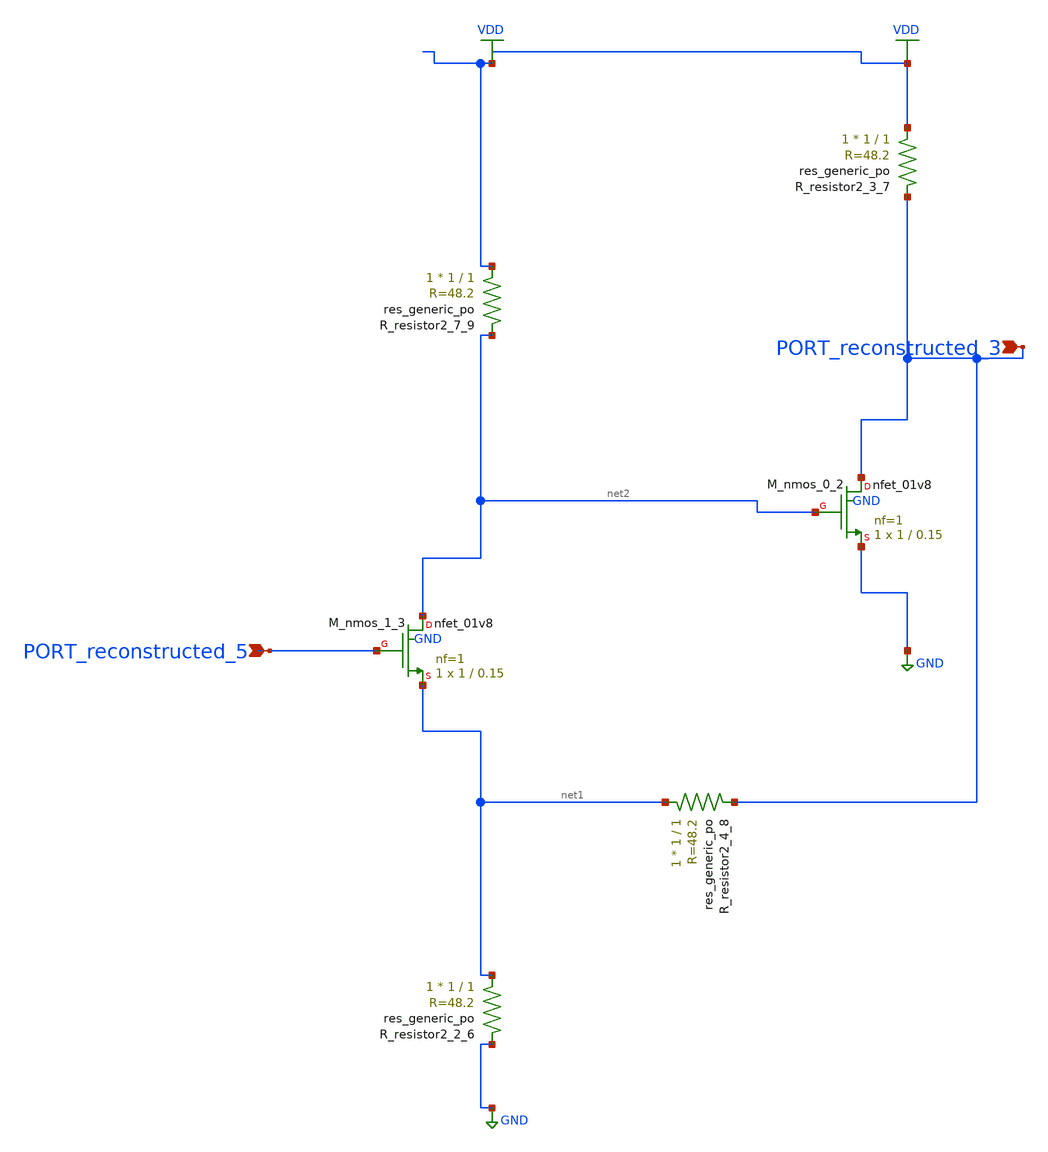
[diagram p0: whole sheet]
** sch_path: schematics/AMSNet/566.sch
**.subckt 566 PORT_reconstructed_3 PORT_reconstructed_5
*.ipin PORT_reconstructed_3
*.ipin PORT_reconstructed_5
XM_nmos_0_2 PORT_reconstructed_3 net2 GND GND sky130_fd_pr__nfet_01v8 L=0.15 W=1 nf=1 ad='int((1 + 1)/2) * 1 / 1 * 0.29'
+ as='int((1 + 2)/2) * 1 / 1 * 0.29' pd='2*int((1 + 1)/2) * (1 / 1 + 0.29)' ps='2*int((1 + 2)/2) * (1 / 1 + 0.29)'
+ nrd='0.29 / 1 ' nrs='0.29 / 1 ' sa=0 sb=0 sd=0 mult=1 m=1
XM_nmos_1_3 net2 PORT_reconstructed_5 net1 GND sky130_fd_pr__nfet_01v8 L=0.15 W=1 nf=1 ad='int((1 + 1)/2) * 1 / 1 * 0.29'
+ as='int((1 + 2)/2) * 1 / 1 * 0.29' pd='2*int((1 + 1)/2) * (1 / 1 + 0.29)' ps='2*int((1 + 2)/2) * (1 / 1 + 0.29)'
+ nrd='0.29 / 1 ' nrs='0.29 / 1 ' sa=0 sb=0 sd=0 mult=1 m=1
XR_resistor2_2_6 net1 GND sky130_fd_pr__res_generic_po W=1 L=1 m=1
XR_resistor2_3_7 VDD PORT_reconstructed_3 sky130_fd_pr__res_generic_po W=1 L=1 m=1
XR_resistor2_4_8 net1 PORT_reconstructed_3 sky130_fd_pr__res_generic_po W=1 L=1 m=1
XR_resistor2_7_9 VDD net2 sky130_fd_pr__res_generic_po W=1 L=1 m=1
**.ends
.GLOBAL GND
.GLOBAL VDD
.end
